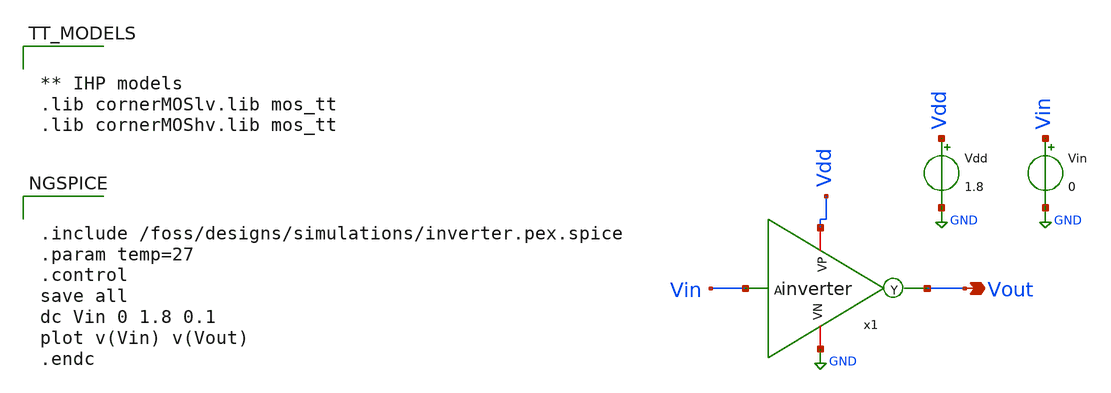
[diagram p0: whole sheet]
** sch_path: inverter/xschem/inverter_tb_dc.sch
**.subckt inverter_tb_dc Vout
*.opin Vout
x1 Vdd Vin Vout GND inverter
Vdd Vdd GND 1.8
Vin Vin GND 0
**** begin user architecture code


** IHP models
.lib cornerMOSlv.lib mos_tt
.lib cornerMOShv.lib mos_tt




.include /foss/designs/simulations/inverter.pex.spice
.param temp=27
.control
save all
dc Vin 0 1.8 0.1
plot v(Vin) v(Vout)
.endc


**** end user architecture code
**.ends
.GLOBAL GND
.end
